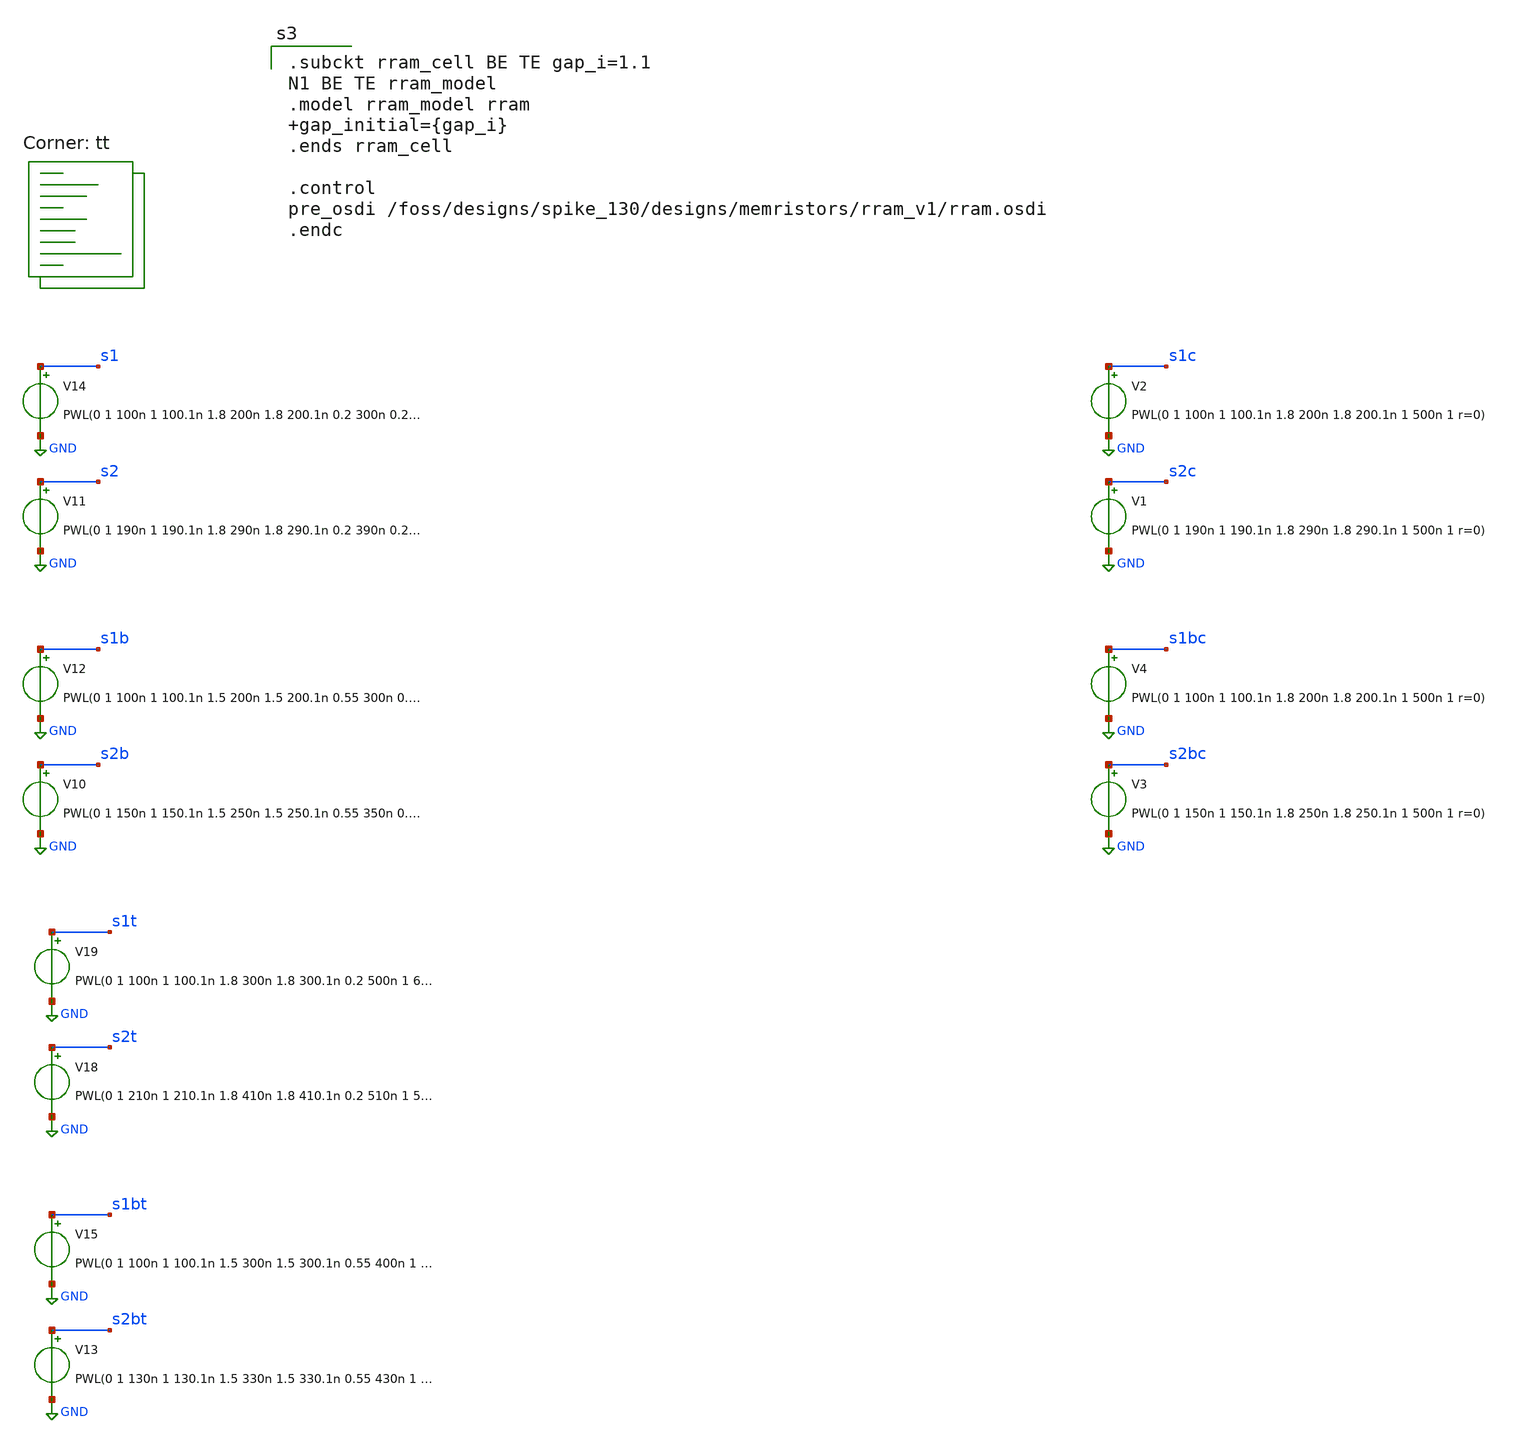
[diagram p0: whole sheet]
** sch_path: designs/tb_2.sch
**.subckt tb_2
V11 s2 GND PWL(0 1 190n 1 190.1n 1.8 290n 1.8 290.1n 0.2 390n 0.2 390.1n 1 500n 1 r=0)
V14 s1 GND PWL(0 1 100n 1 100.1n 1.8 200n 1.8 200.1n 0.2 300n 0.2 300.1n 1 500n 1 r=0)
V10 s2b GND PWL(0 1 150n 1 150.1n 1.5 250n 1.5 250.1n 0.55 350n 0.55 350.1n 1 500n 1 r=0)
V12 s1b GND PWL(0 1 100n 1 100.1n 1.5 200n 1.5 200.1n 0.55 300n 0.55 300.1n 1 500n 1 r=0)
V18 s2t GND PWL(0 1 210n 1 210.1n 1.8 410n 1.8 410.1n 0.2 510n 1 500n 1 r=0)
V19 s1t GND PWL(0 1 100n 1 100.1n 1.8 300n 1.8 300.1n 0.2 500n 1 600n 1 r=0)
V13 s2bt GND PWL(0 1 130n 1 130.1n 1.5 330n 1.5 330.1n 0.55 430n 1 1000n 1 r=0)
V15 s1bt GND PWL(0 1 100n 1 100.1n 1.5 300n 1.5 300.1n 0.55 400n 1 500n 1 r=0)
V1 s2c GND PWL(0 1 190n 1 190.1n 1.8 290n 1.8 290.1n 1 500n 1 r=0)
V2 s1c GND PWL(0 1 100n 1 100.1n 1.8 200n 1.8 200.1n 1 500n 1 r=0)
V3 s2bc GND PWL(0 1 150n 1 150.1n 1.8 250n 1.8 250.1n 1 500n 1 r=0)
V4 s1bc GND PWL(0 1 100n 1 100.1n 1.8 200n 1.8 200.1n 1 500n 1 r=0)
**** begin user architecture code


.control
 set num_threads=16
 tran 10n 5u uic
 write tb_2.raw
.endc
.save all

.lib $::SKYWATER_MODELS/sky130.lib.spice tt

.subckt rram_cell BE TE gap_i=1.1
N1 BE TE rram_model
.model rram_model rram gap_initial={gap_i}
.ends rram_cell

.control
pre_osdi /foss/designs/spike_130/designs/memristors/rram_v1/rram.osdi
.endc

**** end user architecture code
**.ends
.GLOBAL GND
.end
